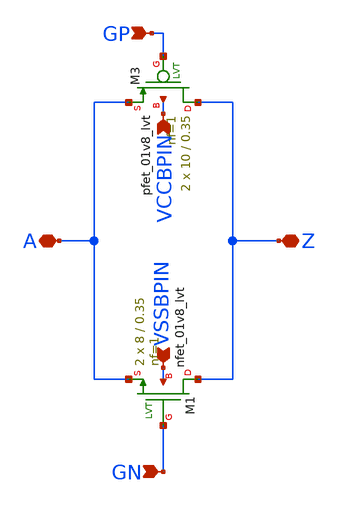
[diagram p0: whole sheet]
** sch_path: xschem/passgate.sch
**.subckt passgate GN VCCBPIN VSSBPIN GP A Z
*.ipin GN
*.ipin VCCBPIN
*.ipin VSSBPIN
*.ipin GP
*.iopin A
*.iopin Z
XM1 Z GN A VSSBPIN sky130_fd_pr__nfet_01v8_lvt L=0.35 W=8 nf=1 ad='int((nf+1)/2) * W/nf * 0.29' as='int((nf+2)/2) * W/nf * 0.29'
+ pd='2*int((nf+1)/2) * (W/nf + 0.29)' ps='2*int((nf+2)/2) * (W/nf + 0.29)' nrd='0.29 / W' nrs='0.29 / W'
+ sa=0 sb=0 sd=0 mult=2 m=2
XM3 Z GP A VCCBPIN sky130_fd_pr__pfet_01v8_lvt L=0.35 W=10 nf=1 ad='int((nf+1)/2) * W/nf * 0.29' as='int((nf+2)/2) * W/nf * 0.29'
+ pd='2*int((nf+1)/2) * (W/nf + 0.29)' ps='2*int((nf+2)/2) * (W/nf + 0.29)' nrd='0.29 / W' nrs='0.29 / W'
+ sa=0 sb=0 sd=0 mult=2 m=2
**.ends
.end
